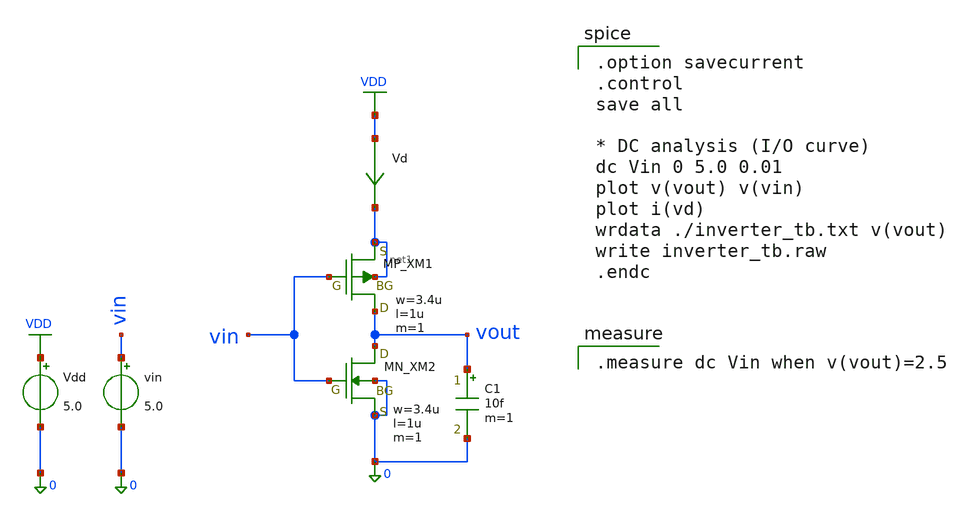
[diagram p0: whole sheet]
** sch_path: inverter/inverter_xu_wenying_tb.sch
**.subckt inverter_xu_wenying_tb
XXM1 vout vin net1 net1 PMOS w=3.4u l=1u nrd=0 nrs=0 m=1
XXM2 vout vin 0 0 NMOS w=3.4u l=1u nrd=0 nrs=0 m=1
Vdd VDD 0 5.0
vin vin 0 5.0
C1 vout 0 10f m=1
Vd VDD net1 0
.save i(vd)
**** begin user architecture code
 .include $::LIB/ip62_models

.option savecurrent
.control
save all

* DC analysis (I/O curve)
dc Vin 0 5.0 0.01
plot v(vout) v(vin)
plot i(vd)
wrdata ./inverter_tb.txt v(vout)
write inverter_tb.raw
.endc


.measure dc Vin when v(vout)=2.5

**** end user architecture code
**.ends
.GLOBAL VDD
.end
